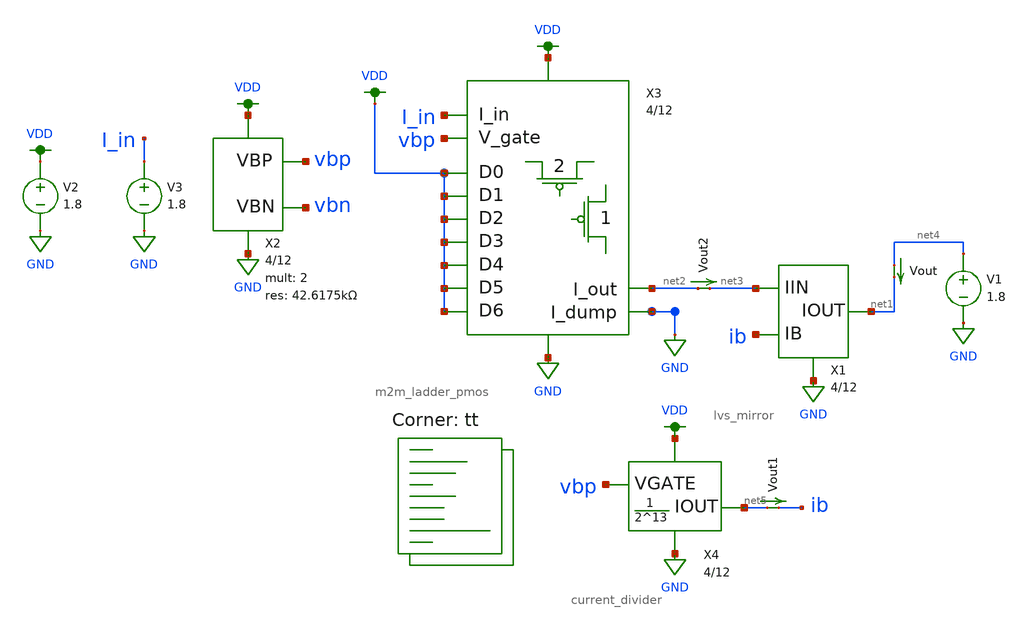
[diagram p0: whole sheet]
** sch_path: dac/schematic/dac_output_voltage_tb.sch
**.subckt dac_output_voltage_tb
V2 VDD GND 1.8
X2 vbp VDD GND vbn bias_gen u_w=4 u_l=12 m=2 r=42.6175k
V3 I_in GND 1.8
X3 VDD GND VDD VDD VDD VDD VDD VDD VDD vbp I_in GND net2 m2m_ladder_pmos u_w=4 u_l=12
Vout2 net2 net3 0
.save i(vout2)
X1 GND net3 ib net1 lvs_mirror u_w=4 u_l=12 m=2 r=1M
Vout net4 net1 0
.save i(vout)
V1 net4 GND 1.8
X4 GND VDD net5 vbp current_divider u_w=4 u_l=12
Vout1 net5 ib 0
.save i(vout1)
**** begin user architecture code


.control
  set wr_vecnames
  set wr_singlescale
  dc V1 0 1.8 0.01
  wrdata ~/documents/git/madvlsi/dac/build/dac_output_voltage/dac_output_voltage_tb.txt i(Vout)
.endc

.lib $::SKYWATER_MODELS/sky130.lib.spice tt
**** end user architecture code
**.ends
.GLOBAL GND
.GLOBAL VDD
.end
